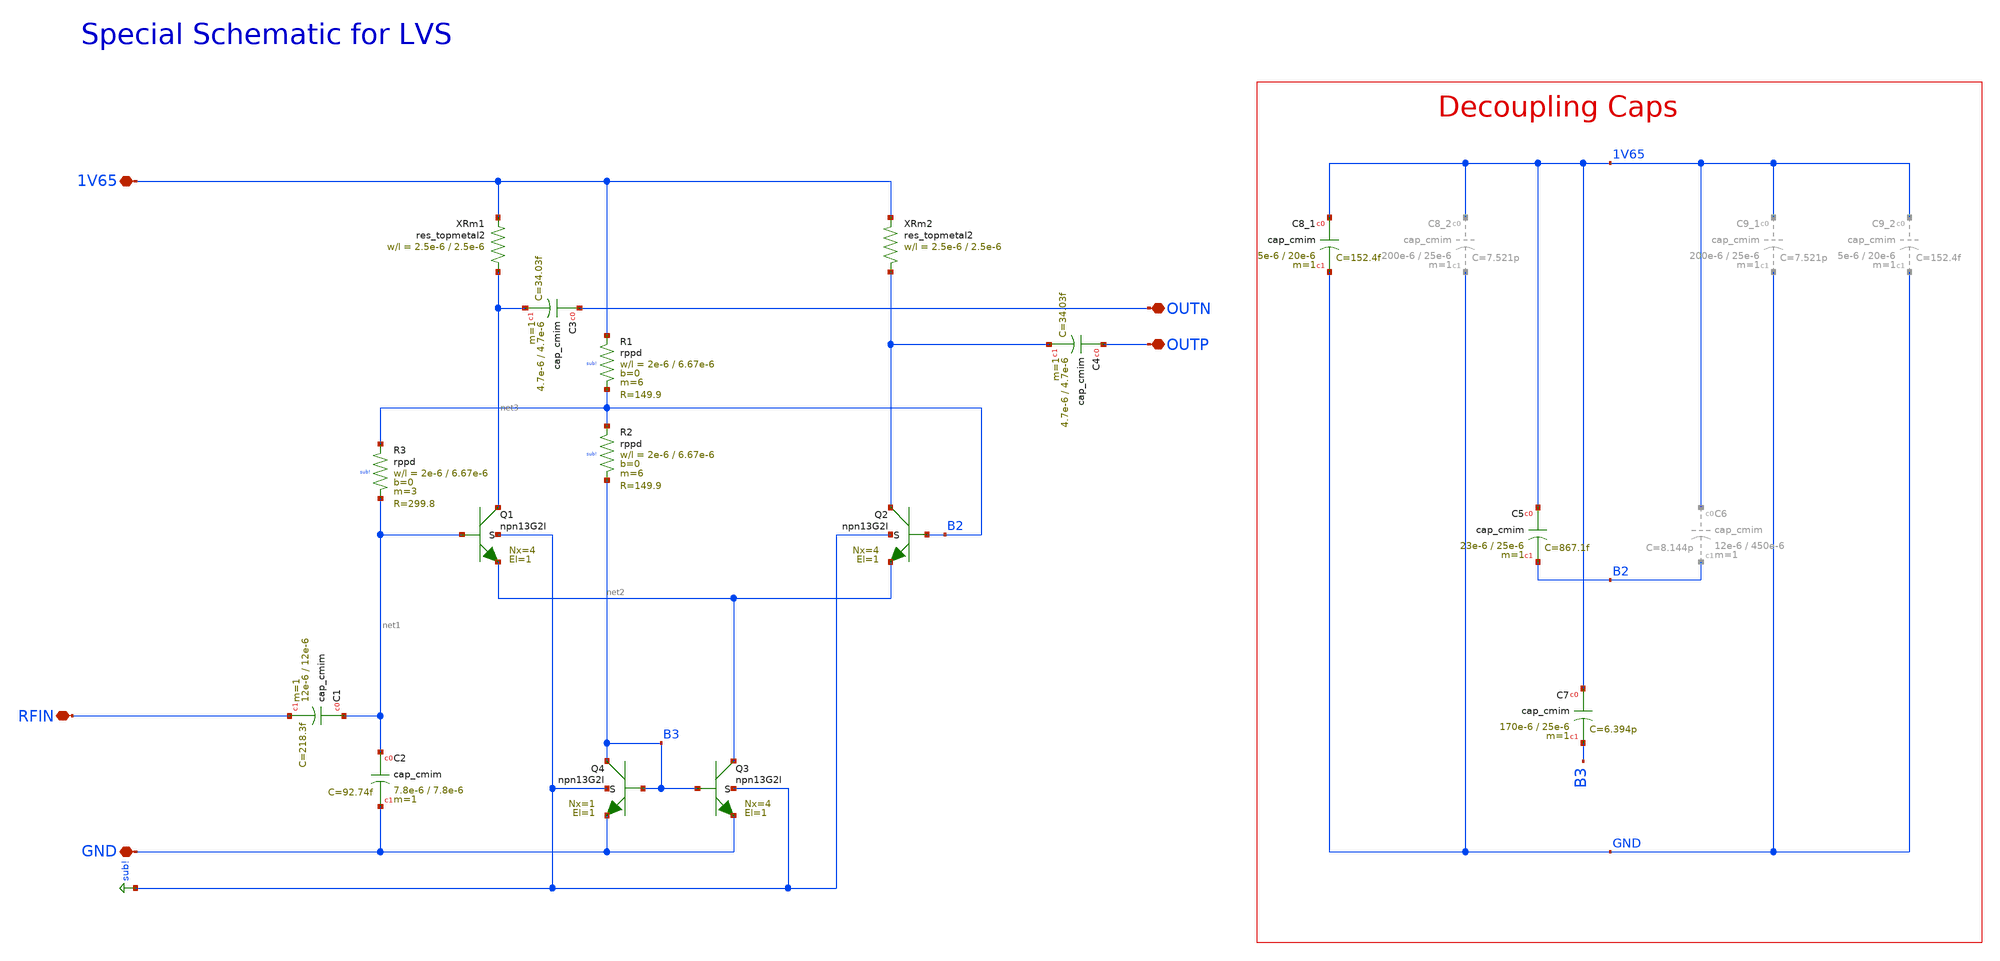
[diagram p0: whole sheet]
** sch_path: mWATTBAT/design_data/lvs/BALUN_MULT_10GSE_50GD_LVS.sch
**.subckt BALUN_MULT_10GSE_50GD_LVS 1V65 GND RFIN OUTN OUTP
*.iopin 1V65
*.iopin GND
*.iopin RFIN
*.iopin OUTN
*.iopin OUTP
XC2 net1 GND cap_cmim w=7.8e-6 l=7.8e-6 m=1 mm_ok=1
XC1 net1 RFIN cap_cmim w=12e-6 l=12e-6 m=1 mm_ok=1
XC3 OUTN net3 cap_cmim w=4.7e-6 l=4.7e-6 m=1 mm_ok=1
XC7 1V65 B3 cap_cmim w=170e-6 l=25e-6 m=1 mm_ok=1
XQ4 B3 B3 GND sub! npn13G2l Nx=1 El=1 mm_ok=1
XQ3 net2 B3 GND sub! npn13G2l Nx=4 El=1 mm_ok=1
XQ1 net3 net1 net2 sub! npn13G2l Nx=4 El=1 mm_ok=1
XQ2 OUTP B2 net2 sub! npn13G2l Nx=4 El=1 mm_ok=1
XC5 1V65 B2 cap_cmim w=23e-6 l=25e-6 m=1 mm_ok=1
XC8_1 1V65 GND cap_cmim w=5e-6 l=20e-6 m=1 mm_ok=1
XR3 B2 net1 sub! rppd w=2e-6 l=6.67e-6 m=3 b=0 mm_ok=1
XR1 1V65 B2 sub! rppd w=2e-6 l=6.67e-6 m=6 b=0 mm_ok=1
XR2 B2 B3 sub! rppd w=2e-6 l=6.67e-6 m=6 b=0 mm_ok=1
XRm1 net3 1V65 res_topmetal2 w=2.5e-6 l=2.5e-6
XRm2 OUTP 1V65 res_topmetal2 w=2.5e-6 l=2.5e-6
**.ends
.GLOBAL sub!
.end
